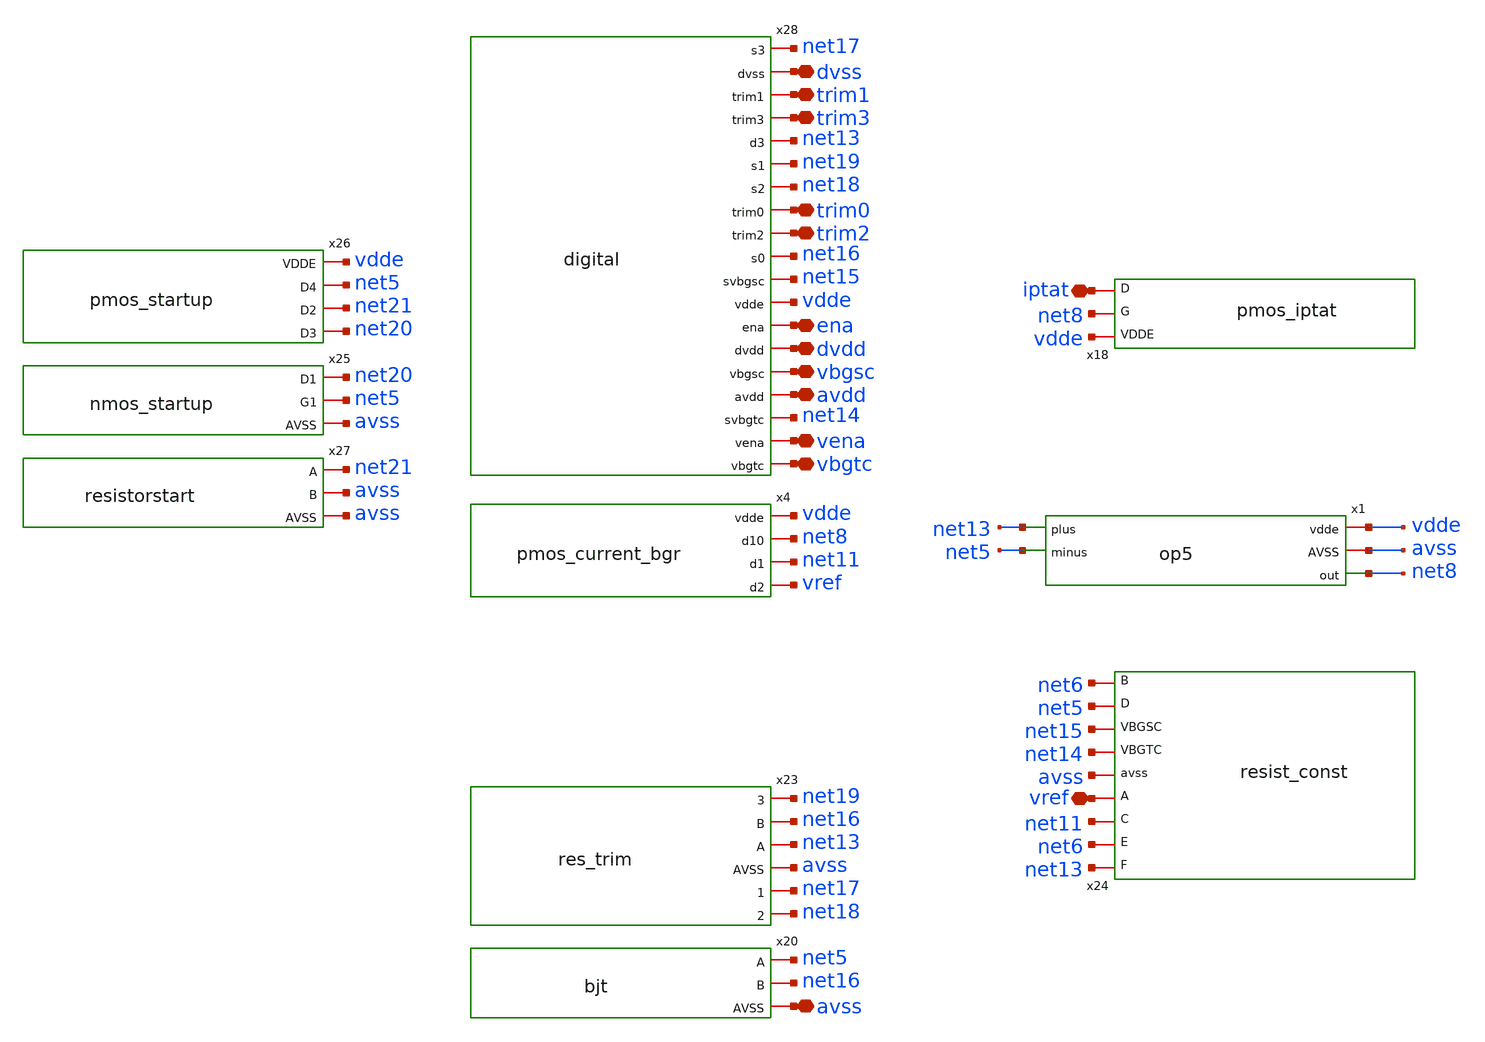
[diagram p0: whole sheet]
** sch_path: magic/bgr_op5_block_rev1.sch
**.subckt bgr_op5_block_rev1 trim1 trim3 trim0 trim2 dvdd vbgsc vbgtc avdd vena ena avss dvss iptat
*+ vref
*.iopin trim1
*.iopin trim3
*.iopin trim0
*.iopin trim2
*.iopin dvdd
*.iopin vbgsc
*.iopin vbgtc
*.iopin avdd
*.iopin vena
*.iopin ena
*.iopin avss
*.iopin dvss
*.iopin iptat
*.iopin vref
x4 vdde net8 net11 vref pmos_current_bgr
x18 vdde net8 iptat pmos_iptat
x20 net5 net16 avss bjt
x23 net19 net16 net13 avss net17 net18 res_trim
x24 net13 net6 net11 vref avss net14 net15 net5 net6 resist_const
x25 net20 net5 avss nmos_startup
x26 vdde net5 net21 net20 pmos_startup
x27 net21 avss avss resistorstart
x28 net17 dvss trim1 trim3 net13 net19 net18 trim0 trim2 net16 net15 vdde ena dvdd vbgsc avdd net14
+ vena vbgtc digital
x1 vdde avss net13 net5 net8 op5
**.ends
.end
